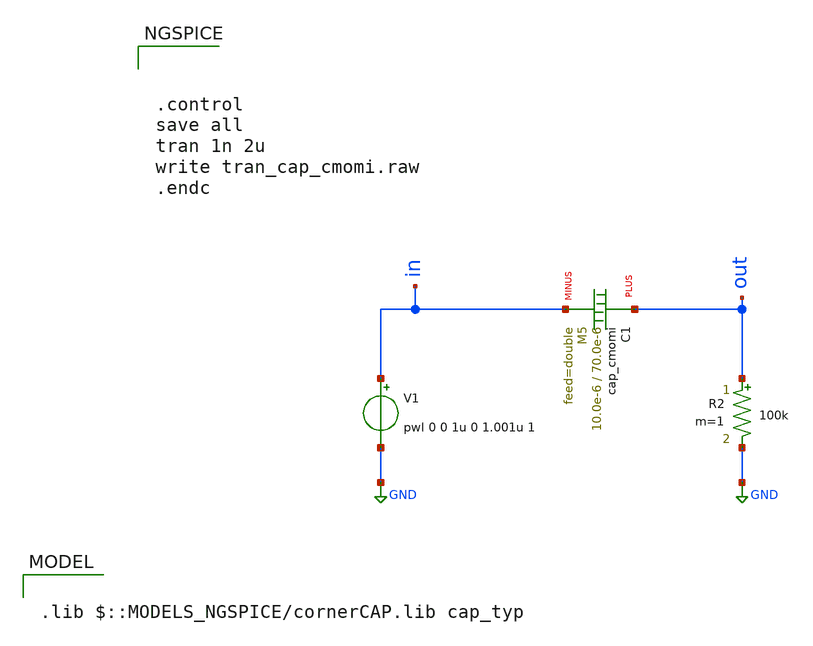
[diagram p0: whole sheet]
** sch_path: ihp-sg13g2/libs.tech/xschem/sg13g2_tests/tran_cap_cmomi.sch
* Copyright 2026 IHP PDK Authors
* Licensed under the Apache License, Version 2.0 (the "License");
* you may not use this file except in compliance with the License.
* You may obtain a copy of the License at
* https://www.apache.org/licenses/LICENSE-2.0
* Unless required by applicable law or agreed to in writing, software
* distributed under the License is distributed on an "AS IS" BASIS,
* WITHOUT WARRANTIES OR CONDITIONS OF ANY KIND, either express or implied.
* See the License for the specific language governing permissions and
* limitations under the License.
**.subckt tran_cap_cmomi
V1 in GND pwl 0 0 1u 0 1.001u 1
R2 out GND 100k m=1
XC1 out in cap_cmomi w=10.0e-6 l=70.0e-6 mmin=1 mmax=5 feed=double subblock=0
**** begin user architecture code



.control
save all
tran 1n 2u
write tran_cap_cmomi.raw
.endc



.lib $::MODELS_NGSPICE/cornerCAP.lib cap_typ

**** end user architecture code
**.ends
.GLOBAL GND
.end
